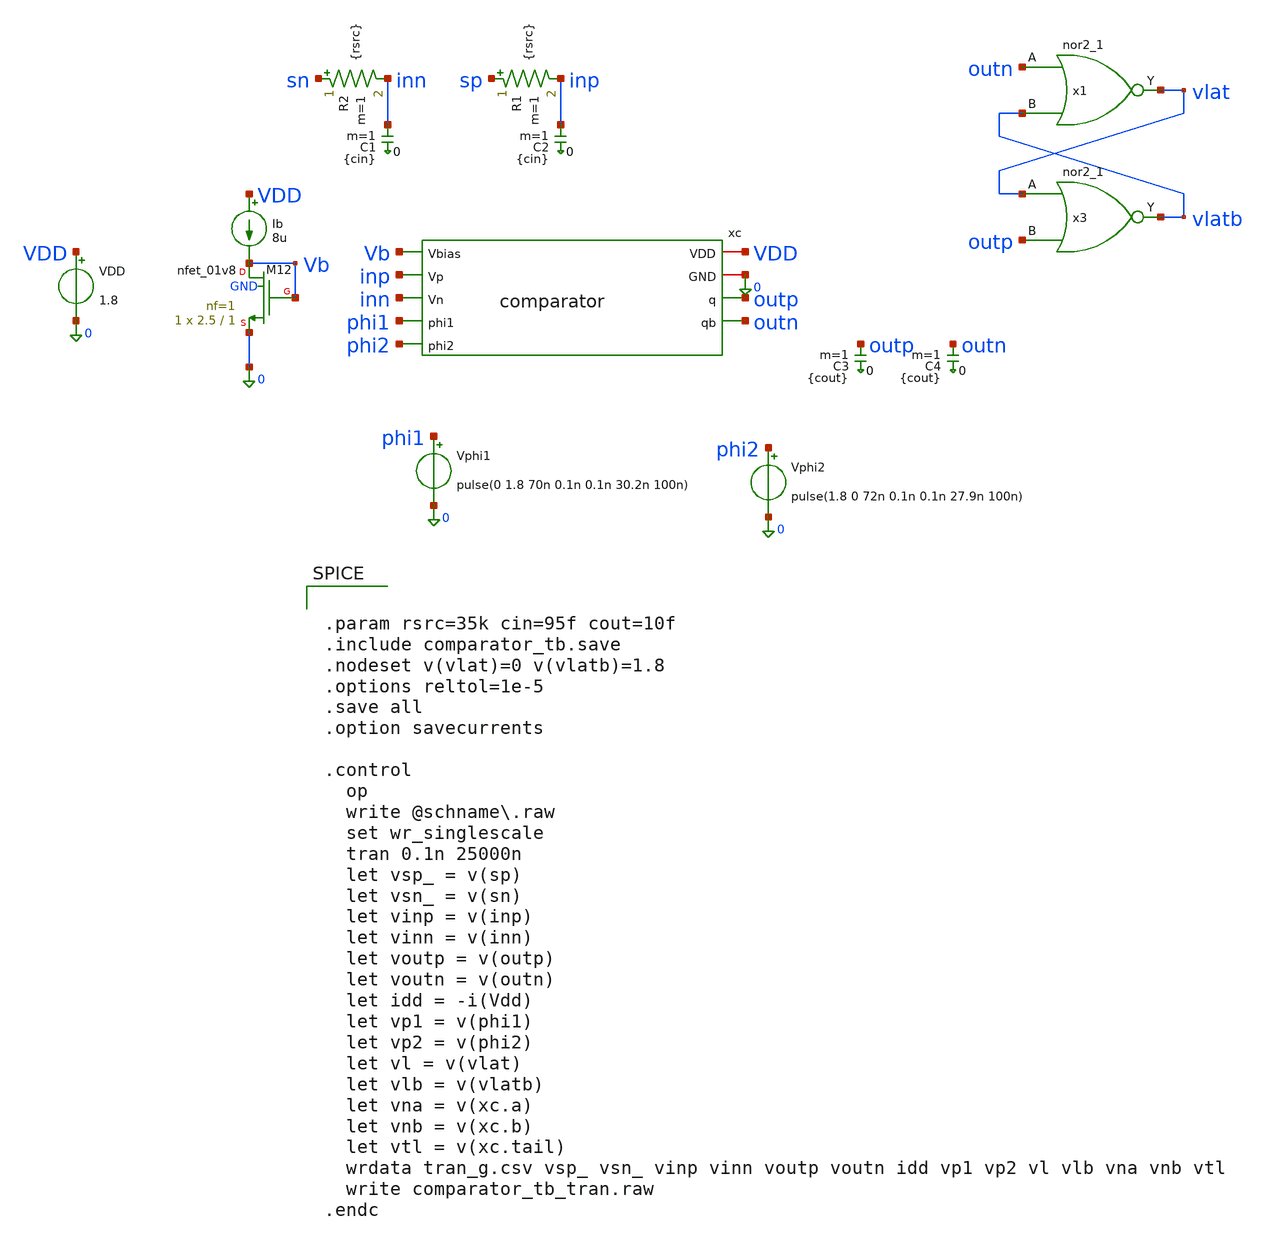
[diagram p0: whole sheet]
** sch_path: sch/comparator/comparator_tb.sch
**.subckt comparator_tb
xc VDD 0 Vb inp inn phi1 phi2 outp outn comparator
VDD VDD 0 1.8
.save i(vdd)
Ib VDD Vb 8u
R1 sp inp {rsrc} m=1
R2 sn inn {rsrc} m=1
C1 inn 0 {cin} m=1
C2 inp 0 {cin} m=1
C3 outp 0 {cout} m=1
C4 outn 0 {cout} m=1
Vphi1 phi1 0 pulse(0 1.8 70n 0.1n 0.1n 30.2n 100n)
.save i(vphi1)
Vphi2 phi2 0 pulse(1.8 0 72n 0.1n 0.1n 27.9n 100n)
.save i(vphi2)
x3 vlat outp 0 0 VDD VDD vlatb sky130_fd_sc_hd__nor2_1
XM12 Vb Vb 0 GND sky130_fd_pr__nfet_01v8 L=1 W=2.5 nf=1 ad='int((1 + 1)/2) * 2.5 / 1 * 0.29' as='int((1 + 2)/2) * 2.5 / 1 * 0.29'
+ pd='2*int((1 + 1)/2) * (2.5 / 1 + 0.29)' ps='2*int((1 + 2)/2) * (2.5 / 1 + 0.29)' nrd='0.29 / 2.5 ' nrs='0.29 / 2.5 '
+ sa=0 sb=0 sd=0 mult=1 m=1
x1 outn vlatb 0 0 VDD VDD vlat sky130_fd_sc_hd__nor2_1
**** begin user architecture code


.param rsrc=35k cin=95f cout=10f
.include comparator_tb.save
.nodeset v(vlat)=0 v(vlatb)=1.8
.options reltol=1e-5
.save all
.option savecurrents

.control
  op
  write @schname\.raw
  set wr_singlescale
  tran 0.1n 25000n
  let vsp_ = v(sp)
  let vsn_ = v(sn)
  let vinp = v(inp)
  let vinn = v(inn)
  let voutp = v(outp)
  let voutn = v(outn)
  let idd = -i(Vdd)
  let vp1 = v(phi1)
  let vp2 = v(phi2)
  let vl = v(vlat)
  let vlb = v(vlatb)
  let vna = v(xc.a)
  let vnb = v(xc.b)
  let vtl = v(xc.tail)
  wrdata tran_g.csv vsp_ vsn_ vinp vinn voutp voutn idd vp1 vp2 vl vlb vna vnb vtl
  write comparator_tb_tran.raw
.endc




Vsp sp 0 pwl( 0.0n 0.9490500 102.0n 0.9490500 102.1n 0.9489500 202.0n 0.9489500 202.1n 0.9491000
+ 302.0n 0.9491000  302.1n 0.9489000 402.0n 0.9489000 402.1n 0.9492500 502.0n 0.9492500 502.1n 0.9487500
+  602.0n 0.9487500 602.1n 0.9495000 702.0n 0.9495000 702.1n 0.9485000 802.0n 0.9485000  802.1n 0.9500000
+ 902.0n 0.9500000 902.1n 0.9480000 1002.0n 0.9480000 1002.1n 0.9515000  1102.0n 0.9515000 1102.1n 0.9465000
+ 1202.0n 0.9465000 1202.1n 0.9540000 1302.0n 0.9540000  1302.1n 0.9440000 1402.0n 0.9440000 1402.1n
+ 0.9590000 1502.0n 0.9590000 1502.1n 0.9390000  1602.0n 0.9390000 1602.1n 0.9740000 1702.0n 0.9740000 1702.1n
+ 0.9240000 1802.0n 0.9240000  1802.1n 0.9990000 1902.0n 0.9990000 1902.1n 0.8990000 2002.0n 0.8990000 2002.1n
+ 0.6025000  2102.0n 0.6025000 2102.1n 0.5975000 2202.0n 0.5975000 2202.1n 0.6005000 2302.0n 0.6005000  2302.1n
+ 0.5995000 2402.0n 0.5995000 2402.1n 0.7025000 2502.0n 0.7025000 2502.1n 0.6975000  2602.0n 0.6975000 2602.1n
+ 0.7005000 2702.0n 0.7005000 2702.1n 0.6995000 2802.0n 0.6995000  2802.1n 0.8025000 2902.0n 0.8025000 2902.1n
+ 0.7975000 3002.0n 0.7975000 3002.1n 0.8005000  3102.0n 0.8005000 3102.1n 0.7995000 3202.0n 0.7995000 3202.1n
+ 0.9025000 3302.0n 0.9025000  3302.1n 0.8975000 3402.0n 0.8975000 3402.1n 0.9005000 3502.0n 0.9005000 3502.1n
+ 0.8995000  3602.0n 0.8995000 3602.1n 0.9515000 3702.0n 0.9515000 3702.1n 0.9465000 3802.0n 0.9465000  3802.1n
+ 0.9495000 3902.0n 0.9495000 3902.1n 0.9485000 4002.0n 0.9485000 4002.1n 1.0025000  4102.0n 1.0025000 4102.1n
+ 0.9975000 4202.0n 0.9975000 4202.1n 1.0005000 4302.0n 1.0005000  4302.1n 0.9995000 4402.0n 0.9995000 4402.1n
+ 1.1025000 4502.0n 1.1025000 4502.1n 1.0975000  4602.0n 1.0975000 4602.1n 1.1005000 4702.0n 1.1005000 4702.1n
+ 1.0995000 4802.0n 1.0995000  4802.1n 1.2025000 4902.0n 1.2025000 4902.1n 1.1975000 5002.0n 1.1975000 5002.1n
+ 1.2005000  5102.0n 1.2005000 5102.1n 1.1995000 5202.0n 1.1995000 5202.1n 1.3025000 5302.0n 1.3025000  5302.1n
+ 1.2975000 5402.0n 1.2975000 5402.1n 1.3005000 5502.0n 1.3005000 5502.1n 1.2995000  5602.0n 1.2995000 5602.1n
+ 0.9430000 5702.0n 0.9430000 5702.1n 0.9431250 5802.0n 0.9431250  5802.1n 0.9432500 5902.0n 0.9432500 5902.1n
+ 0.9433750 6002.0n 0.9433750 6002.1n 0.9435000  6102.0n 0.9435000 6102.1n 0.9436250 6202.0n 0.9436250 6202.1n
+ 0.9437500 6302.0n 0.9437500  6302.1n 0.9438750 6402.0n 0.9438750 6402.1n 0.9440000 6502.0n 0.9440000 6502.1n
+ 0.9441250  6602.0n 0.9441250 6602.1n 0.9442500 6702.0n 0.9442500 6702.1n 0.9443750 6802.0n 0.9443750  6802.1n
+ 0.9445000 6902.0n 0.9445000 6902.1n 0.9446250 7002.0n 0.9446250 7002.1n 0.9447500  7102.0n 0.9447500 7102.1n
+ 0.9448750 7202.0n 0.9448750 7202.1n 0.9450000 7302.0n 0.9450000  7302.1n 0.9451250 7402.0n 0.9451250 7402.1n
+ 0.9452500 7502.0n 0.9452500 7502.1n 0.9453750  7602.0n 0.9453750 7602.1n 0.9455000 7702.0n 0.9455000 7702.1n
+ 0.9456250 7802.0n 0.9456250  7802.1n 0.9457500 7902.0n 0.9457500 7902.1n 0.9458750 8002.0n 0.9458750 8002.1n
+ 0.9460000  8102.0n 0.9460000 8102.1n 0.9461250 8202.0n 0.9461250 8202.1n 0.9462500 8302.0n 0.9462500  8302.1n
+ 0.9463750 8402.0n 0.9463750 8402.1n 0.9465000 8502.0n 0.9465000 8502.1n 0.9466250  8602.0n 0.9466250 8602.1n
+ 0.9467500 8702.0n 0.9467500 8702.1n 0.9468750 8802.0n 0.9468750  8802.1n 0.9470000 8902.0n 0.9470000 8902.1n
+ 0.9471250 9002.0n 0.9471250 9002.1n 0.9472500  9102.0n 0.9472500 9102.1n 0.9473750 9202.0n 0.9473750 9202.1n
+ 0.9475000 9302.0n 0.9475000  9302.1n 0.9476250 9402.0n 0.9476250 9402.1n 0.9477500 9502.0n 0.9477500 9502.1n
+ 0.9478750  9602.0n 0.9478750 9602.1n 0.9480000 9702.0n 0.9480000 9702.1n 0.9481250 9802.0n 0.9481250  9802.1n
+ 0.9482500 9902.0n 0.9482500 9902.1n 0.9483750 10002.0n 0.9483750 10002.1n 0.9485000  10102.0n 0.9485000
+ 10102.1n 0.9486250 10202.0n 0.9486250 10202.1n 0.9487500 10302.0n 0.9487500  10302.1n 0.9488750 10402.0n
+ 0.9488750 10402.1n 0.9490000 10502.0n 0.9490000 10502.1n 0.9491250  10602.0n 0.9491250 10602.1n 0.9492500
+ 10702.0n 0.9492500 10702.1n 0.9493750 10802.0n 0.9493750  10802.1n 0.9495000 10902.0n 0.9495000 10902.1n
+ 0.9496250 11002.0n 0.9496250 11002.1n 0.9497500  11102.0n 0.9497500 11102.1n 0.9498750 11202.0n 0.9498750
+ 11202.1n 0.9500000 11302.0n 0.9500000  11302.1n 0.9501250 11402.0n 0.9501250 11402.1n 0.9502500 11502.0n
+ 0.9502500 11502.1n 0.9503750  11602.0n 0.9503750 11602.1n 0.9505000 11702.0n 0.9505000 11702.1n 0.9506250
+ 11802.0n 0.9506250  11802.1n 0.9507500 11902.0n 0.9507500 11902.1n 0.9508750 12002.0n 0.9508750 12002.1n
+ 0.9510000  12102.0n 0.9510000 12102.1n 0.9511250 12202.0n 0.9511250 12202.1n 0.9512500 12302.0n 0.9512500
+  12302.1n 0.9513750 12402.0n 0.9513750 12402.1n 0.9515000 12502.0n 0.9515000 12502.1n 0.9516250  12602.0n
+ 0.9516250 12602.1n 0.9517500 12702.0n 0.9517500 12702.1n 0.9518750 12802.0n 0.9518750  12802.1n 0.9520000
+ 12902.0n 0.9520000 12902.1n 0.9521250 13002.0n 0.9521250 13002.1n 0.9522500  13102.0n 0.9522500 13102.1n
+ 0.9523750 13202.0n 0.9523750 13202.1n 0.9525000 13302.0n 0.9525000  13302.1n 0.9526250 13402.0n 0.9526250
+ 13402.1n 0.9527500 13502.0n 0.9527500 13502.1n 0.9528750  13602.0n 0.9528750 13602.1n 0.9530000 13702.0n
+ 0.9530000 13702.1n 0.9531250 13802.0n 0.9531250  13802.1n 0.9532500 13902.0n 0.9532500 13902.1n 0.9533750
+ 14002.0n 0.9533750 14002.1n 0.9535000  14102.0n 0.9535000 14102.1n 0.9536250 14202.0n 0.9536250 14202.1n
+ 0.9537500 14302.0n 0.9537500  14302.1n 0.9538750 14402.0n 0.9538750 14402.1n 0.9540000 14502.0n 0.9540000
+ 14502.1n 0.9541250  14602.0n 0.9541250 14602.1n 0.9542500 14702.0n 0.9542500 14702.1n 0.9543750 14802.0n
+ 0.9543750  14802.1n 0.9545000 14902.0n 0.9545000 14902.1n 0.9546250 15002.0n 0.9546250 15002.1n 0.9547500
+  15102.0n 0.9547500 15102.1n 0.9548750 15202.0n 0.9548750 15202.1n 0.9550000 15302.0n 0.9550000  15302.1n
+ 0.9550000 15402.0n 0.9550000 15402.1n 0.9548750 15502.0n 0.9548750 15502.1n 0.9547500  15602.0n 0.9547500
+ 15602.1n 0.9546250 15702.0n 0.9546250 15702.1n 0.9545000 15802.0n 0.9545000  15802.1n 0.9543750 15902.0n
+ 0.9543750 15902.1n 0.9542500 16002.0n 0.9542500 16002.1n 0.9541250  16102.0n 0.9541250 16102.1n 0.9540000
+ 16202.0n 0.9540000 16202.1n 0.9538750 16302.0n 0.9538750  16302.1n 0.9537500 16402.0n 0.9537500 16402.1n
+ 0.9536250 16502.0n 0.9536250 16502.1n 0.9535000  16602.0n 0.9535000 16602.1n 0.9533750 16702.0n 0.9533750
+ 16702.1n 0.9532500 16802.0n 0.9532500  16802.1n 0.9531250 16902.0n 0.9531250 16902.1n 0.9530000 17002.0n
+ 0.9530000 17002.1n 0.9528750  17102.0n 0.9528750 17102.1n 0.9527500 17202.0n 0.9527500 17202.1n 0.9526250
+ 17302.0n 0.9526250  17302.1n 0.9525000 17402.0n 0.9525000 17402.1n 0.9523750 17502.0n 0.9523750 17502.1n
+ 0.9522500  17602.0n 0.9522500 17602.1n 0.9521250 17702.0n 0.9521250 17702.1n 0.9520000 17802.0n 0.9520000
+  17802.1n 0.9518750 17902.0n 0.9518750 17902.1n 0.9517500 18002.0n 0.9517500 18002.1n 0.9516250  18102.0n
+ 0.9516250 18102.1n 0.9515000 18202.0n 0.9515000 18202.1n 0.9513750 18302.0n 0.9513750  18302.1n 0.9512500
+ 18402.0n 0.9512500 18402.1n 0.9511250 18502.0n 0.9511250 18502.1n 0.9510000  18602.0n 0.9510000 18602.1n
+ 0.9508750 18702.0n 0.9508750 18702.1n 0.9507500 18802.0n 0.9507500  18802.1n 0.9506250 18902.0n 0.9506250
+ 18902.1n 0.9505000 19002.0n 0.9505000 19002.1n 0.9503750  19102.0n 0.9503750 19102.1n 0.9502500 19202.0n
+ 0.9502500 19202.1n 0.9501250 19302.0n 0.9501250  19302.1n 0.9500000 19402.0n 0.9500000 19402.1n 0.9498750
+ 19502.0n 0.9498750 19502.1n 0.9497500  19602.0n 0.9497500 19602.1n 0.9496250 19702.0n 0.9496250 19702.1n
+ 0.9495000 19802.0n 0.9495000  19802.1n 0.9493750 19902.0n 0.9493750 19902.1n 0.9492500 20002.0n 0.9492500
+ 20002.1n 0.9491250  20102.0n 0.9491250 20102.1n 0.9490000 20202.0n 0.9490000 20202.1n 0.9488750 20302.0n
+ 0.9488750  20302.1n 0.9487500 20402.0n 0.9487500 20402.1n 0.9486250 20502.0n 0.9486250 20502.1n 0.9485000
+  20602.0n 0.9485000 20602.1n 0.9483750 20702.0n 0.9483750 20702.1n 0.9482500 20802.0n 0.9482500  20802.1n
+ 0.9481250 20902.0n 0.9481250 20902.1n 0.9480000 21002.0n 0.9480000 21002.1n 0.9478750  21102.0n 0.9478750
+ 21102.1n 0.9477500 21202.0n 0.9477500 21202.1n 0.9476250 21302.0n 0.9476250  21302.1n 0.9475000 21402.0n
+ 0.9475000 21402.1n 0.9473750 21502.0n 0.9473750 21502.1n 0.9472500  21602.0n 0.9472500 21602.1n 0.9471250
+ 21702.0n 0.9471250 21702.1n 0.9470000 21802.0n 0.9470000  21802.1n 0.9468750 21902.0n 0.9468750 21902.1n
+ 0.9467500 22002.0n 0.9467500 22002.1n 0.9466250  22102.0n 0.9466250 22102.1n 0.9465000 22202.0n 0.9465000
+ 22202.1n 0.9463750 22302.0n 0.9463750  22302.1n 0.9462500 22402.0n 0.9462500 22402.1n 0.9461250 22502.0n
+ 0.9461250 22502.1n 0.9460000  22602.0n 0.9460000 22602.1n 0.9458750 22702.0n 0.9458750 22702.1n 0.9457500
+ 22802.0n 0.9457500  22802.1n 0.9456250 22902.0n 0.9456250 22902.1n 0.9455000 23002.0n 0.9455000 23002.1n
+ 0.9453750  23102.0n 0.9453750 23102.1n 0.9452500 23202.0n 0.9452500 23202.1n 0.9451250 23302.0n 0.9451250
+  23302.1n 0.9450000 23402.0n 0.9450000 23402.1n 0.9448750 23502.0n 0.9448750 23502.1n 0.9447500  23602.0n
+ 0.9447500 23602.1n 0.9446250 23702.0n 0.9446250 23702.1n 0.9445000 23802.0n 0.9445000  23802.1n 0.9443750
+ 23902.0n 0.9443750 23902.1n 0.9442500 24002.0n 0.9442500 24002.1n 0.9441250  24102.0n 0.9441250 24102.1n
+ 0.9440000 24202.0n 0.9440000 24202.1n 0.9438750 24302.0n 0.9438750  24302.1n 0.9437500 24402.0n 0.9437500
+ 24402.1n 0.9436250 24502.0n 0.9436250 24502.1n 0.9435000  24602.0n 0.9435000 24602.1n 0.9433750 24702.0n
+ 0.9433750 24702.1n 0.9432500 24802.0n 0.9432500  24802.1n 0.9431250 24902.0n 0.9431250 24902.1n 0.9430000
+ 25000.0n 0.9430000)
Vsn sn 0 pwl( 0.0n 0.9489500 102.0n 0.9489500 102.1n 0.9490500 202.0n 0.9490500 202.1n 0.9489000
+ 302.0n 0.9489000  302.1n 0.9491000 402.0n 0.9491000 402.1n 0.9487500 502.0n 0.9487500 502.1n 0.9492500
+  602.0n 0.9492500 602.1n 0.9485000 702.0n 0.9485000 702.1n 0.9495000 802.0n 0.9495000  802.1n 0.9480000
+ 902.0n 0.9480000 902.1n 0.9500000 1002.0n 0.9500000 1002.1n 0.9465000  1102.0n 0.9465000 1102.1n 0.9515000
+ 1202.0n 0.9515000 1202.1n 0.9440000 1302.0n 0.9440000  1302.1n 0.9540000 1402.0n 0.9540000 1402.1n
+ 0.9390000 1502.0n 0.9390000 1502.1n 0.9590000  1602.0n 0.9590000 1602.1n 0.9240000 1702.0n 0.9240000 1702.1n
+ 0.9740000 1802.0n 0.9740000  1802.1n 0.8990000 1902.0n 0.8990000 1902.1n 0.9990000 2002.0n 0.9990000 2002.1n
+ 0.5975000  2102.0n 0.5975000 2102.1n 0.6025000 2202.0n 0.6025000 2202.1n 0.5995000 2302.0n 0.5995000  2302.1n
+ 0.6005000 2402.0n 0.6005000 2402.1n 0.6975000 2502.0n 0.6975000 2502.1n 0.7025000  2602.0n 0.7025000 2602.1n
+ 0.6995000 2702.0n 0.6995000 2702.1n 0.7005000 2802.0n 0.7005000  2802.1n 0.7975000 2902.0n 0.7975000 2902.1n
+ 0.8025000 3002.0n 0.8025000 3002.1n 0.7995000  3102.0n 0.7995000 3102.1n 0.8005000 3202.0n 0.8005000 3202.1n
+ 0.8975000 3302.0n 0.8975000  3302.1n 0.9025000 3402.0n 0.9025000 3402.1n 0.8995000 3502.0n 0.8995000 3502.1n
+ 0.9005000  3602.0n 0.9005000 3602.1n 0.9465000 3702.0n 0.9465000 3702.1n 0.9515000 3802.0n 0.9515000  3802.1n
+ 0.9485000 3902.0n 0.9485000 3902.1n 0.9495000 4002.0n 0.9495000 4002.1n 0.9975000  4102.0n 0.9975000 4102.1n
+ 1.0025000 4202.0n 1.0025000 4202.1n 0.9995000 4302.0n 0.9995000  4302.1n 1.0005000 4402.0n 1.0005000 4402.1n
+ 1.0975000 4502.0n 1.0975000 4502.1n 1.1025000  4602.0n 1.1025000 4602.1n 1.0995000 4702.0n 1.0995000 4702.1n
+ 1.1005000 4802.0n 1.1005000  4802.1n 1.1975000 4902.0n 1.1975000 4902.1n 1.2025000 5002.0n 1.2025000 5002.1n
+ 1.1995000  5102.0n 1.1995000 5102.1n 1.2005000 5202.0n 1.2005000 5202.1n 1.2975000 5302.0n 1.2975000  5302.1n
+ 1.3025000 5402.0n 1.3025000 5402.1n 1.2995000 5502.0n 1.2995000 5502.1n 1.3005000  5602.0n 1.3005000 5602.1n
+ 0.9550000 5702.0n 0.9550000 5702.1n 0.9548750 5802.0n 0.9548750  5802.1n 0.9547500 5902.0n 0.9547500 5902.1n
+ 0.9546250 6002.0n 0.9546250 6002.1n 0.9545000  6102.0n 0.9545000 6102.1n 0.9543750 6202.0n 0.9543750 6202.1n
+ 0.9542500 6302.0n 0.9542500  6302.1n 0.9541250 6402.0n 0.9541250 6402.1n 0.9540000 6502.0n 0.9540000 6502.1n
+ 0.9538750  6602.0n 0.9538750 6602.1n 0.9537500 6702.0n 0.9537500 6702.1n 0.9536250 6802.0n 0.9536250  6802.1n
+ 0.9535000 6902.0n 0.9535000 6902.1n 0.9533750 7002.0n 0.9533750 7002.1n 0.9532500  7102.0n 0.9532500 7102.1n
+ 0.9531250 7202.0n 0.9531250 7202.1n 0.9530000 7302.0n 0.9530000  7302.1n 0.9528750 7402.0n 0.9528750 7402.1n
+ 0.9527500 7502.0n 0.9527500 7502.1n 0.9526250  7602.0n 0.9526250 7602.1n 0.9525000 7702.0n 0.9525000 7702.1n
+ 0.9523750 7802.0n 0.9523750  7802.1n 0.9522500 7902.0n 0.9522500 7902.1n 0.9521250 8002.0n 0.9521250 8002.1n
+ 0.9520000  8102.0n 0.9520000 8102.1n 0.9518750 8202.0n 0.9518750 8202.1n 0.9517500 8302.0n 0.9517500  8302.1n
+ 0.9516250 8402.0n 0.9516250 8402.1n 0.9515000 8502.0n 0.9515000 8502.1n 0.9513750  8602.0n 0.9513750 8602.1n
+ 0.9512500 8702.0n 0.9512500 8702.1n 0.9511250 8802.0n 0.9511250  8802.1n 0.9510000 8902.0n 0.9510000 8902.1n
+ 0.9508750 9002.0n 0.9508750 9002.1n 0.9507500  9102.0n 0.9507500 9102.1n 0.9506250 9202.0n 0.9506250 9202.1n
+ 0.9505000 9302.0n 0.9505000  9302.1n 0.9503750 9402.0n 0.9503750 9402.1n 0.9502500 9502.0n 0.9502500 9502.1n
+ 0.9501250  9602.0n 0.9501250 9602.1n 0.9500000 9702.0n 0.9500000 9702.1n 0.9498750 9802.0n 0.9498750  9802.1n
+ 0.9497500 9902.0n 0.9497500 9902.1n 0.9496250 10002.0n 0.9496250 10002.1n 0.9495000  10102.0n 0.9495000
+ 10102.1n 0.9493750 10202.0n 0.9493750 10202.1n 0.9492500 10302.0n 0.9492500  10302.1n 0.9491250 10402.0n
+ 0.9491250 10402.1n 0.9490000 10502.0n 0.9490000 10502.1n 0.9488750  10602.0n 0.9488750 10602.1n 0.9487500
+ 10702.0n 0.9487500 10702.1n 0.9486250 10802.0n 0.9486250  10802.1n 0.9485000 10902.0n 0.9485000 10902.1n
+ 0.9483750 11002.0n 0.9483750 11002.1n 0.9482500  11102.0n 0.9482500 11102.1n 0.9481250 11202.0n 0.9481250
+ 11202.1n 0.9480000 11302.0n 0.9480000  11302.1n 0.9478750 11402.0n 0.9478750 11402.1n 0.9477500 11502.0n
+ 0.9477500 11502.1n 0.9476250  11602.0n 0.9476250 11602.1n 0.9475000 11702.0n 0.9475000 11702.1n 0.9473750
+ 11802.0n 0.9473750  11802.1n 0.9472500 11902.0n 0.9472500 11902.1n 0.9471250 12002.0n 0.9471250 12002.1n
+ 0.9470000  12102.0n 0.9470000 12102.1n 0.9468750 12202.0n 0.9468750 12202.1n 0.9467500 12302.0n 0.9467500
+  12302.1n 0.9466250 12402.0n 0.9466250 12402.1n 0.9465000 12502.0n 0.9465000 12502.1n 0.9463750  12602.0n
+ 0.9463750 12602.1n 0.9462500 12702.0n 0.9462500 12702.1n 0.9461250 12802.0n 0.9461250  12802.1n 0.9460000
+ 12902.0n 0.9460000 12902.1n 0.9458750 13002.0n 0.9458750 13002.1n 0.9457500  13102.0n 0.9457500 13102.1n
+ 0.9456250 13202.0n 0.9456250 13202.1n 0.9455000 13302.0n 0.9455000  13302.1n 0.9453750 13402.0n 0.9453750
+ 13402.1n 0.9452500 13502.0n 0.9452500 13502.1n 0.9451250  13602.0n 0.9451250 13602.1n 0.9450000 13702.0n
+ 0.9450000 13702.1n 0.9448750 13802.0n 0.9448750  13802.1n 0.9447500 13902.0n 0.9447500 13902.1n 0.9446250
+ 14002.0n 0.9446250 14002.1n 0.9445000  14102.0n 0.9445000 14102.1n 0.9443750 14202.0n 0.9443750 14202.1n
+ 0.9442500 14302.0n 0.9442500  14302.1n 0.9441250 14402.0n 0.9441250 14402.1n 0.9440000 14502.0n 0.9440000
+ 14502.1n 0.9438750  14602.0n 0.9438750 14602.1n 0.9437500 14702.0n 0.9437500 14702.1n 0.9436250 14802.0n
+ 0.9436250  14802.1n 0.9435000 14902.0n 0.9435000 14902.1n 0.9433750 15002.0n 0.9433750 15002.1n 0.9432500
+  15102.0n 0.9432500 15102.1n 0.9431250 15202.0n 0.9431250 15202.1n 0.9430000 15302.0n 0.9430000  15302.1n
+ 0.9430000 15402.0n 0.9430000 15402.1n 0.9431250 15502.0n 0.9431250 15502.1n 0.9432500  15602.0n 0.9432500
+ 15602.1n 0.9433750 15702.0n 0.9433750 15702.1n 0.9435000 15802.0n 0.9435000  15802.1n 0.9436250 15902.0n
+ 0.9436250 15902.1n 0.9437500 16002.0n 0.9437500 16002.1n 0.9438750  16102.0n 0.9438750 16102.1n 0.9440000
+ 16202.0n 0.9440000 16202.1n 0.9441250 16302.0n 0.9441250  16302.1n 0.9442500 16402.0n 0.9442500 16402.1n
+ 0.9443750 16502.0n 0.9443750 16502.1n 0.9445000  16602.0n 0.9445000 16602.1n 0.9446250 16702.0n 0.9446250
+ 16702.1n 0.9447500 16802.0n 0.9447500  16802.1n 0.9448750 16902.0n 0.9448750 16902.1n 0.9450000 17002.0n
+ 0.9450000 17002.1n 0.9451250  17102.0n 0.9451250 17102.1n 0.9452500 17202.0n 0.9452500 17202.1n 0.9453750
+ 17302.0n 0.9453750  17302.1n 0.9455000 17402.0n 0.9455000 17402.1n 0.9456250 17502.0n 0.9456250 17502.1n
+ 0.9457500  17602.0n 0.9457500 17602.1n 0.9458750 17702.0n 0.9458750 17702.1n 0.9460000 17802.0n 0.9460000
+  17802.1n 0.9461250 17902.0n 0.9461250 17902.1n 0.9462500 18002.0n 0.9462500 18002.1n 0.9463750  18102.0n
+ 0.9463750 18102.1n 0.9465000 18202.0n 0.9465000 18202.1n 0.9466250 18302.0n 0.9466250  18302.1n 0.9467500
+ 18402.0n 0.9467500 18402.1n 0.9468750 18502.0n 0.9468750 18502.1n 0.9470000  18602.0n 0.9470000 18602.1n
+ 0.9471250 18702.0n 0.9471250 18702.1n 0.9472500 18802.0n 0.9472500  18802.1n 0.9473750 18902.0n 0.9473750
+ 18902.1n 0.9475000 19002.0n 0.9475000 19002.1n 0.9476250  19102.0n 0.9476250 19102.1n 0.9477500 19202.0n
+ 0.9477500 19202.1n 0.9478750 19302.0n 0.9478750  19302.1n 0.9480000 19402.0n 0.9480000 19402.1n 0.9481250
+ 19502.0n 0.9481250 19502.1n 0.9482500  19602.0n 0.9482500 19602.1n 0.9483750 19702.0n 0.9483750 19702.1n
+ 0.9485000 19802.0n 0.9485000  19802.1n 0.9486250 19902.0n 0.9486250 19902.1n 0.9487500 20002.0n 0.9487500
+ 20002.1n 0.9488750  20102.0n 0.9488750 20102.1n 0.9490000 20202.0n 0.9490000 20202.1n 0.9491250 20302.0n
+ 0.9491250  20302.1n 0.9492500 20402.0n 0.9492500 20402.1n 0.9493750 20502.0n 0.9493750 20502.1n 0.9495000
+  20602.0n 0.9495000 20602.1n 0.9496250 20702.0n 0.9496250 20702.1n 0.9497500 20802.0n 0.9497500  20802.1n
+ 0.9498750 20902.0n 0.9498750 20902.1n 0.9500000 21002.0n 0.9500000 21002.1n 0.9501250  21102.0n 0.9501250
+ 21102.1n 0.9502500 21202.0n 0.9502500 21202.1n 0.9503750 21302.0n 0.9503750  21302.1n 0.9505000 21402.0n
+ 0.9505000 21402.1n 0.9506250 21502.0n 0.9506250 21502.1n 0.9507500  21602.0n 0.9507500 21602.1n 0.9508750
+ 21702.0n 0.9508750 21702.1n 0.9510000 21802.0n 0.9510000  21802.1n 0.9511250 21902.0n 0.9511250 21902.1n
+ 0.9512500 22002.0n 0.9512500 22002.1n 0.9513750  22102.0n 0.9513750 22102.1n 0.9515000 22202.0n 0.9515000
+ 22202.1n 0.9516250 22302.0n 0.9516250  22302.1n 0.9517500 22402.0n 0.9517500 22402.1n 0.9518750 22502.0n
+ 0.9518750 22502.1n 0.9520000  22602.0n 0.9520000 22602.1n 0.9521250 22702.0n 0.9521250 22702.1n 0.9522500
+ 22802.0n 0.9522500  22802.1n 0.9523750 22902.0n 0.9523750 22902.1n 0.9525000 23002.0n 0.9525000 23002.1n
+ 0.9526250  23102.0n 0.9526250 23102.1n 0.9527500 23202.0n 0.9527500 23202.1n 0.9528750 23302.0n 0.9528750
+  23302.1n 0.9530000 23402.0n 0.9530000 23402.1n 0.9531250 23502.0n 0.9531250 23502.1n 0.9532500  23602.0n
+ 0.9532500 23602.1n 0.9533750 23702.0n 0.9533750 23702.1n 0.9535000 23802.0n 0.9535000  23802.1n 0.9536250
+ 23902.0n 0.9536250 23902.1n 0.9537500 24002.0n 0.9537500 24002.1n 0.9538750  24102.0n 0.9538750 24102.1n
+ 0.9540000 24202.0n 0.9540000 24202.1n 0.9541250 24302.0n 0.9541250  24302.1n 0.9542500 24402.0n 0.9542500
+ 24402.1n 0.9543750 24502.0n 0.9543750 24502.1n 0.9545000  24602.0n 0.9545000 24602.1n 0.9546250 24702.0n
+ 0.9546250 24702.1n 0.9547500 24802.0n 0.9547500  24802.1n 0.9548750 24902.0n 0.9548750 24902.1n 0.9550000
+ 25000.0n 0.9550000)



** opencircuitdesign pdks install
.lib $::SKYWATER_MODELS/sky130.lib.spice tt
.include $::SKYWATER_STDCELLS/sky130_fd_sc_hd.spice

**** end user architecture code
**.ends

* expanding   symbol:  /foss/designs/sar_adc/sch/comparator/comparator.sym # of pins=9
** sym_path: sch/comparator/comparator.sym
** sch_path: sch/comparator/comparator.sch
.subckt comparator VDD GND Vbias Vp Vn phi1 phi2 q qb
*.ipin Vbias
*.opin q
*.iopin VDD
*.iopin GND
*.ipin Vp
*.ipin Vn
*.opin qb
*.ipin phi1
*.ipin phi2
XM1 a Vn tail GND sky130_fd_pr__nfet_01v8 L=0.5 W=4.15 nf=1 ad='int((1 + 1)/2) * 4.15 / 1 * 0.29' as='int((1 + 2)/2) * 4.15 / 1 * 0.29'
+ pd='2*int((1 + 1)/2) * (4.15 / 1 + 0.29)' ps='2*int((1 + 2)/2) * (4.15 / 1 + 0.29)' nrd='0.29 / 4.15 '
+ nrs='0.29 / 4.15 ' sa=0 sb=0 sd=0 mult=1 m=1
XM2 b Vp tail GND sky130_fd_pr__nfet_01v8 L=0.5 W=4.15 nf=1 ad='int((1 + 1)/2) * 4.15 / 1 * 0.29' as='int((1 + 2)/2) * 4.15 / 1 * 0.29'
+ pd='2*int((1 + 1)/2) * (4.15 / 1 + 0.29)' ps='2*int((1 + 2)/2) * (4.15 / 1 + 0.29)' nrd='0.29 / 4.15 '
+ nrs='0.29 / 4.15 ' sa=0 sb=0 sd=0 mult=1 m=1
XM12 tail Vbias GND GND sky130_fd_pr__nfet_01v8 L=1 W=4.3 nf=1 ad='int((1 + 1)/2) * 4.3 / 1 * 0.29' as='int((1 + 2)/2) * 4.3 / 1 * 0.29'
+ pd='2*int((1 + 1)/2) * (4.3 / 1 + 0.29)' ps='2*int((1 + 2)/2) * (4.3 / 1 + 0.29)' nrd='0.29 / 4.3 ' nrs='0.29 / 4.3 '
+ sa=0 sb=0 sd=0 mult=1 m=1
XM10 q phi2 GND GND sky130_fd_pr__nfet_01v8 L=0.15 W=1 nf=1 ad='int((1 + 1)/2) * 1 / 1 * 0.29' as='int((1 + 2)/2) * 1 / 1 * 0.29'
+ pd='2*int((1 + 1)/2) * (1 / 1 + 0.29)' ps='2*int((1 + 2)/2) * (1 / 1 + 0.29)' nrd='0.29 / 1 ' nrs='0.29 / 1 '
+ sa=0 sb=0 sd=0 mult=1 m=1
XM5 q qb GND GND sky130_fd_pr__nfet_01v8 L=1 W=0.5 nf=1 ad='int((1 + 1)/2) * 0.5 / 1 * 0.29' as='int((1 + 2)/2) * 0.5 / 1 * 0.29'
+ pd='2*int((1 + 1)/2) * (0.5 / 1 + 0.29)' ps='2*int((1 + 2)/2) * (0.5 / 1 + 0.29)' nrd='0.29 / 0.5 ' nrs='0.29 / 0.5 '
+ sa=0 sb=0 sd=0 mult=1 m=1
XM6 qb q GND GND sky130_fd_pr__nfet_01v8 L=1 W=0.5 nf=1 ad='int((1 + 1)/2) * 0.5 / 1 * 0.29' as='int((1 + 2)/2) * 0.5 / 1 * 0.29'
+ pd='2*int((1 + 1)/2) * (0.5 / 1 + 0.29)' ps='2*int((1 + 2)/2) * (0.5 / 1 + 0.29)' nrd='0.29 / 0.5 ' nrs='0.29 / 0.5 '
+ sa=0 sb=0 sd=0 mult=1 m=1
XM11 qb phi2 GND GND sky130_fd_pr__nfet_01v8 L=0.15 W=1 nf=1 ad='int((1 + 1)/2) * 1 / 1 * 0.29' as='int((1 + 2)/2) * 1 / 1 * 0.29'
+ pd='2*int((1 + 1)/2) * (1 / 1 + 0.29)' ps='2*int((1 + 2)/2) * (1 / 1 + 0.29)' nrd='0.29 / 1 ' nrs='0.29 / 1 '
+ sa=0 sb=0 sd=0 mult=1 m=1
XM8 qb phi2 b VDD sky130_fd_pr__pfet_01v8 L=0.15 W=1 nf=1 ad='int((1 + 1)/2) * 1 / 1 * 0.29' as='int((1 + 2)/2) * 1 / 1 * 0.29'
+ pd='2*int((1 + 1)/2) * (1 / 1 + 0.29)' ps='2*int((1 + 2)/2) * (1 / 1 + 0.29)' nrd='0.29 / 1 ' nrs='0.29 / 1 '
+ sa=0 sb=0 sd=0 mult=1 m=1
XM7 q phi2 a VDD sky130_fd_pr__pfet_01v8 L=0.15 W=1 nf=1 ad='int((1 + 1)/2) * 1 / 1 * 0.29' as='int((1 + 2)/2) * 1 / 1 * 0.29'
+ pd='2*int((1 + 1)/2) * (1 / 1 + 0.29)' ps='2*int((1 + 2)/2) * (1 / 1 + 0.29)' nrd='0.29 / 1 ' nrs='0.29 / 1 '
+ sa=0 sb=0 sd=0 mult=1 m=1
XM3 a b VDD VDD sky130_fd_pr__pfet_01v8_lvt L=0.5 W=1 nf=1 ad='int((1 + 1)/2) * 1 / 1 * 0.29' as='int((1 + 2)/2) * 1 / 1 * 0.29'
+ pd='2*int((1 + 1)/2) * (1 / 1 + 0.29)' ps='2*int((1 + 2)/2) * (1 / 1 + 0.29)' nrd='0.29 / 1 ' nrs='0.29 / 1 '
+ sa=0 sb=0 sd=0 mult=1 m=1
XM4 b a VDD VDD sky130_fd_pr__pfet_01v8_lvt L=0.5 W=1 nf=1 ad='int((1 + 1)/2) * 1 / 1 * 0.29' as='int((1 + 2)/2) * 1 / 1 * 0.29'
+ pd='2*int((1 + 1)/2) * (1 / 1 + 0.29)' ps='2*int((1 + 2)/2) * (1 / 1 + 0.29)' nrd='0.29 / 1 ' nrs='0.29 / 1 '
+ sa=0 sb=0 sd=0 mult=1 m=1
XM9 a phi1 b VDD sky130_fd_pr__pfet_01v8_lvt L=0.35 W=1 nf=1 ad='int((1 + 1)/2) * 1 / 1 * 0.29' as='int((1 + 2)/2) * 1 / 1 * 0.29'
+ pd='2*int((1 + 1)/2) * (1 / 1 + 0.29)' ps='2*int((1 + 2)/2) * (1 / 1 + 0.29)' nrd='0.29 / 1 ' nrs='0.29 / 1 '
+ sa=0 sb=0 sd=0 mult=1 m=1
.ends

.end
